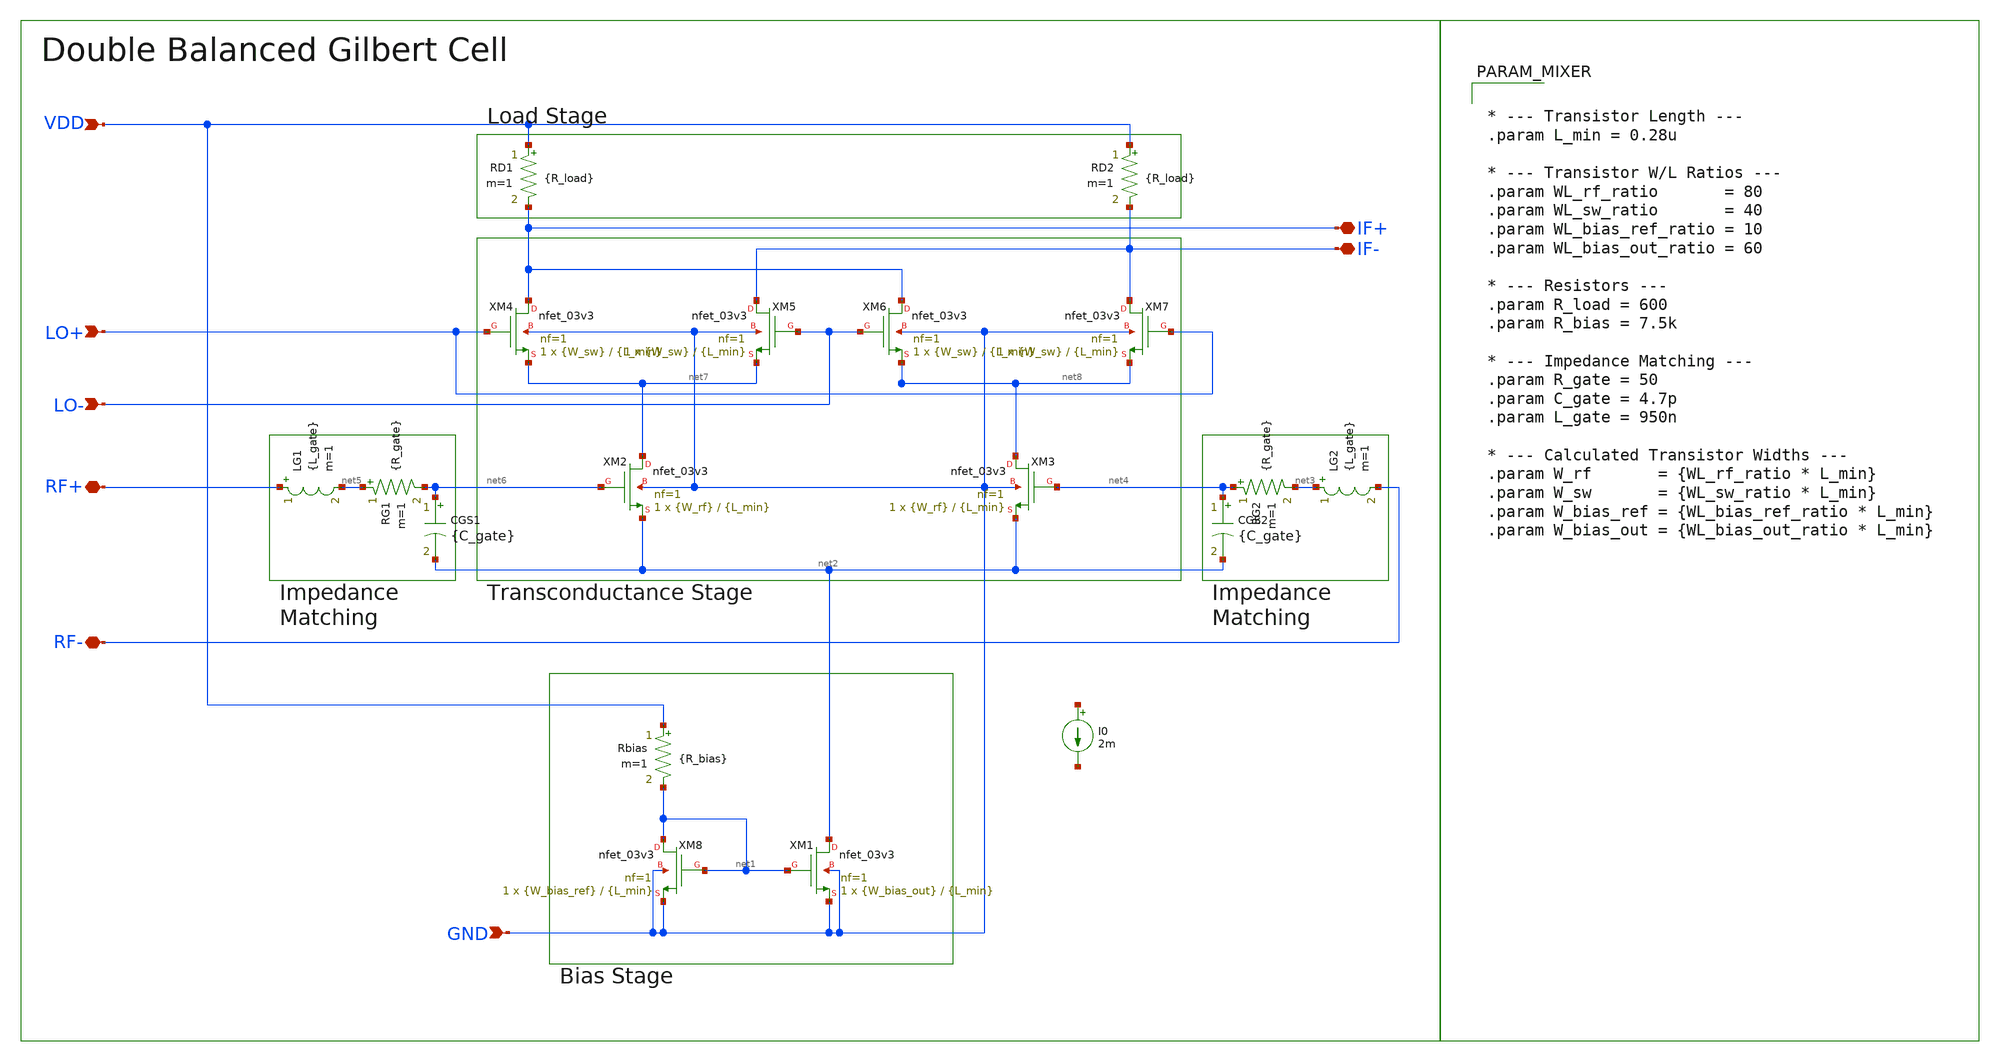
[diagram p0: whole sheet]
** sch_path: Project/1-on-chip/schematic/Mixer/Mixer.sch
**.subckt Mixer GND VDD LO+ LO- RF+ RF- IF+ IF-
*.ipin GND
*.ipin VDD
*.ipin LO+
*.ipin LO-
*.iopin RF+
*.iopin RF-
*.iopin IF+
*.iopin IF-
XM8 net1 net1 GND GND nfet_03v3 L={L_min} W={W_bias_ref} nf=1 ad='int((nf+1)/2) * W/nf * 0.18u' as='int((nf+2)/2) * W/nf * 0.18u'
+ pd='2*int((nf+1)/2) * (W/nf + 0.18u)' ps='2*int((nf+2)/2) * (W/nf + 0.18u)' nrd='0.18u / W' nrs='0.18u / W'
+ sa=0 sb=0 sd=0 m=1
XM1 net2 net1 GND GND nfet_03v3 L={L_min} W={W_bias_out} nf=1 ad='int((nf+1)/2) * W/nf * 0.18u' as='int((nf+2)/2) * W/nf * 0.18u'
+ pd='2*int((nf+1)/2) * (W/nf + 0.18u)' ps='2*int((nf+2)/2) * (W/nf + 0.18u)' nrd='0.18u / W' nrs='0.18u / W'
+ sa=0 sb=0 sd=0 m=1
XM3 net8 net4 net2 GND nfet_03v3 L={L_min} W={W_rf} nf=1 ad='int((nf+1)/2) * W/nf * 0.18u' as='int((nf+2)/2) * W/nf * 0.18u'
+ pd='2*int((nf+1)/2) * (W/nf + 0.18u)' ps='2*int((nf+2)/2) * (W/nf + 0.18u)' nrd='0.18u / W' nrs='0.18u / W'
+ sa=0 sb=0 sd=0 m=1
XM2 net7 net6 net2 GND nfet_03v3 L={L_min} W={W_rf} nf=1 ad='int((nf+1)/2) * W/nf * 0.18u' as='int((nf+2)/2) * W/nf * 0.18u'
+ pd='2*int((nf+1)/2) * (W/nf + 0.18u)' ps='2*int((nf+2)/2) * (W/nf + 0.18u)' nrd='0.18u / W' nrs='0.18u / W'
+ sa=0 sb=0 sd=0 m=1
CGS2 net4 net2 {C_gate} m=1
LG2 net3 RF- {L_gate} m=1
CGS1 net6 net2 {C_gate} m=1
LG1 RF+ net5 {L_gate} m=1
RG1 net5 net6 {R_gate} m=1
RG2 net4 net3 {R_gate} m=1
XM7 IF- LO+ net8 GND nfet_03v3 L={L_min} W={W_sw} nf=1 ad='int((nf+1)/2) * W/nf * 0.18u' as='int((nf+2)/2) * W/nf * 0.18u'
+ pd='2*int((nf+1)/2) * (W/nf + 0.18u)' ps='2*int((nf+2)/2) * (W/nf + 0.18u)' nrd='0.18u / W' nrs='0.18u / W'
+ sa=0 sb=0 sd=0 m=1
XM6 IF+ LO- net8 GND nfet_03v3 L={L_min} W={W_sw} nf=1 ad='int((nf+1)/2) * W/nf * 0.18u' as='int((nf+2)/2) * W/nf * 0.18u'
+ pd='2*int((nf+1)/2) * (W/nf + 0.18u)' ps='2*int((nf+2)/2) * (W/nf + 0.18u)' nrd='0.18u / W' nrs='0.18u / W'
+ sa=0 sb=0 sd=0 m=1
XM5 IF- LO- net7 GND nfet_03v3 L={L_min} W={W_sw} nf=1 ad='int((nf+1)/2) * W/nf * 0.18u' as='int((nf+2)/2) * W/nf * 0.18u'
+ pd='2*int((nf+1)/2) * (W/nf + 0.18u)' ps='2*int((nf+2)/2) * (W/nf + 0.18u)' nrd='0.18u / W' nrs='0.18u / W'
+ sa=0 sb=0 sd=0 m=1
XM4 IF+ LO+ net7 GND nfet_03v3 L={L_min} W={W_sw} nf=1 ad='int((nf+1)/2) * W/nf * 0.18u' as='int((nf+2)/2) * W/nf * 0.18u'
+ pd='2*int((nf+1)/2) * (W/nf + 0.18u)' ps='2*int((nf+2)/2) * (W/nf + 0.18u)' nrd='0.18u / W' nrs='0.18u / W'
+ sa=0 sb=0 sd=0 m=1
RD2 VDD IF- {R_load} m=1
RD1 VDD IF+ {R_load} m=1
Rbias VDD net1 {R_bias} m=1
I0 net9 net10 2m
**** begin user architecture code


* --- Transistor Length ---
.param L_min = 0.28u

* --- Transistor W/L Ratios ---
.param WL_rf_ratio       = 80
.param WL_sw_ratio       = 40
.param WL_bias_ref_ratio = 10
.param WL_bias_out_ratio = 60

* --- Resistors ---
.param R_load = 600
.param R_bias = 7.5k

* --- Impedance Matching ---
.param R_gate = 50
.param C_gate = 4.7p
.param L_gate = 950n

* --- Calculated Transistor Widths ---
.param W_rf       = {WL_rf_ratio * L_min}
.param W_sw       = {WL_sw_ratio * L_min}
.param W_bias_ref = {WL_bias_ref_ratio * L_min}
.param W_bias_out = {WL_bias_out_ratio * L_min}




**** end user architecture code
**.ends
.end
